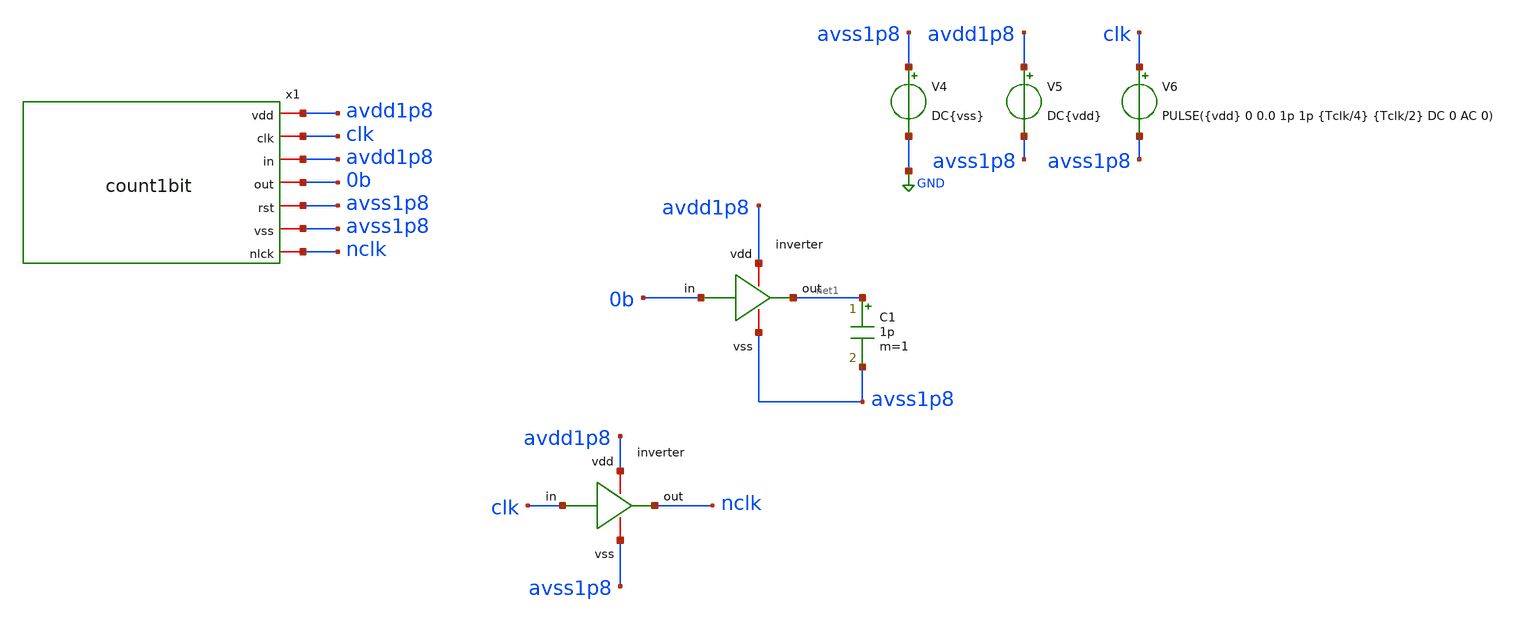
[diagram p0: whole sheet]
** sch_path: verification/testbenches/tb_count.sch
**.subckt tb_count
C1 net1 avss1p8 1p m=1
V4 avss1p8 GND DC{vss}
V5 avdd1p8 avss1p8 DC{vdd}
V6 clk avss1p8 PULSE({vdd} 0 0.0 1p 1p {Tclk/4} {Tclk/2} DC 0 AC 0)
x2 avdd1p8 net1 0b avss1p8 inverter
x3 avdd1p8 nclk clk avss1p8 inverter
x1 avdd1p8 clk avdd1p8 0b avss1p8 avss1p8 nclk count1bit
**** begin user architecture code


* Circuit Parameters
.param vdd = 1.2
.param vss = 0.0
.param Tclk = 10n
.options TEMP = 27.0
* Include Models - IHP SG13G2
.lib cornerMOSlv.lib mos_tt
* OP Parameters & Singals to save
.save all
*Simulations
.control
tran 0.01u 100n
setplot tran1
plot v(clk) v(0b)+1.2
reset
dc V6 0 1.2 0.01
setplot dc
set filetype = ascii
write dcsweep.raw
.endc
.end


**** end user architecture code
**.ends
.GLOBAL GND
.end
